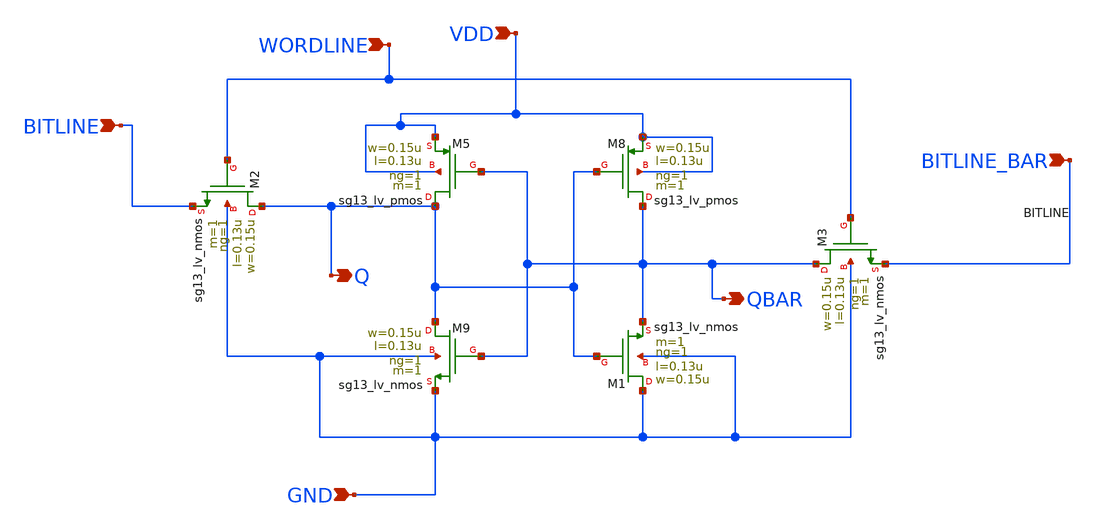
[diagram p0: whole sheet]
** sch_path: projetofinal/shared/schematic_sram/SRAM_symbol.sch
**.subckt SRAM_symbol BITLINE Q BITLINE_BAR VDD WORDLINE GND QBAR
*.ipin BITLINE
*.opin Q
*.ipin BITLINE_BAR
*.ipin VDD
*.ipin WORDLINE
*.ipin GND
*.opin QBAR
XM5 Q QBAR VDD VDD sg13_lv_pmos w=0.15u l=0.13u ng=1 m=1 mm_ok=1
XM9 Q QBAR GND GND sg13_lv_nmos w=0.15u l=0.13u ng=1 m=1 mm_ok=1
XM8 QBAR Q VDD VDD sg13_lv_pmos w=0.15u l=0.13u ng=1 m=1 mm_ok=1
XM1 GND Q QBAR GND sg13_lv_nmos w=0.15u l=0.13u ng=1 m=1 mm_ok=1
XM2 Q WORDLINE BITLINE GND sg13_lv_nmos w=0.15u l=0.13u ng=1 m=1 mm_ok=1
XM3 QBAR WORDLINE BITLINE_BAR GND sg13_lv_nmos w=0.15u l=0.13u ng=1 m=1 mm_ok=1
**.ends
.end
